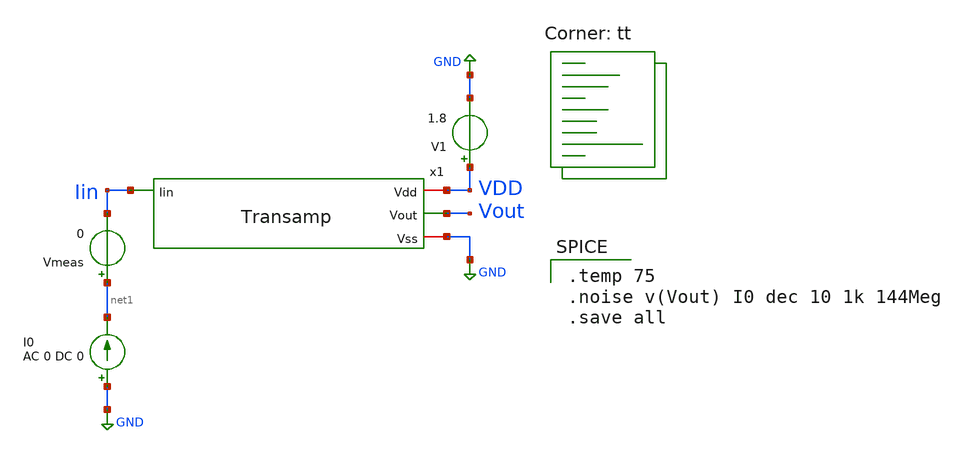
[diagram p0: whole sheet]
** sch_path: analog/library/TIAs/RGC-TIA/TIA_noise_tb.sch
**.subckt TIA_noise_tb
x1 VDD Vout Iin GND Transamp
V1 VDD GND 1.8
I0 GND net1 AC 0 DC 0
Vmeas net1 Iin 0
.save i(vmeas)
**** begin user architecture code
.lib $::SKYWATER_MODELS/sky130.lib.spice tt

.temp 75
.noise v(Vout) I0 dec 10 1k 144Meg
.save all

**** end user architecture code
**.ends

* expanding   symbol:  Transamp.sym # of pins=4
** sym_path: analog/library/TIAs/RGC-TIA/Transamp.sym
** sch_path: analog/library/TIAs/RGC-TIA/Transamp.sch
.subckt Transamp Vdd Vout Iin Vss
*.ipin Iin
*.opin Vout
*.iopin Vss
*.iopin Vdd
R1 net1 Vdd sky130_fd_pr__res_generic_l1 W=0.20 L=32.8 m=1
R2 net2 Vdd sky130_fd_pr__res_generic_l1 W=0.20 L=32.8 m=1
R4 Vss Iin sky130_fd_pr__res_generic_l1 W=0.20 L=32.8 m=1
XM1 net1 net2 Iin Iin sky130_fd_pr__nfet_01v8_lvt L=0.5 W='12.5 * 10 ' nf=10 ad='int((10 + 1)/2) * 12.5 / 10 * 0.29'
+ as='int((10 + 2)/2) * 12.5 / 10 * 0.29' pd='2*int((10 + 1)/2) * (12.5 / 10 + 0.29)' ps='2*int((10 + 2)/2) * (12.5 / 10 + 0.29)'
+ nrd='0.29 / 12.5 ' nrs='0.29 / 12.5 ' sa=0 sb=0 sd=0 mult=1 m=1
XM2 net2 Iin Vss Vss sky130_fd_pr__nfet_01v8_lvt L=0.5 W='12.5 * 10 ' nf=10 ad='int((10 + 1)/2) * 12.5 / 10 * 0.29'
+ as='int((10 + 2)/2) * 12.5 / 10 * 0.29' pd='2*int((10 + 1)/2) * (12.5 / 10 + 0.29)' ps='2*int((10 + 2)/2) * (12.5 / 10 + 0.29)'
+ nrd='0.29 / 12.5 ' nrs='0.29 / 12.5 ' sa=0 sb=0 sd=0 mult=1 m=1
R3 Vout Vdd sky130_fd_pr__res_generic_l1 W=0.20 L=98.3 m=1
XM3 Vout net1 net3 net3 sky130_fd_pr__nfet_01v8_lvt L=0.5 W='12.5 * 10 ' nf=10 ad='int((10 + 1)/2) * 12.5 / 10 * 0.29'
+ as='int((10 + 2)/2) * 12.5 / 10 * 0.29' pd='2*int((10 + 1)/2) * (12.5 / 10 + 0.29)' ps='2*int((10 + 2)/2) * (12.5 / 10 + 0.29)'
+ nrd='0.29 / 12.5 ' nrs='0.29 / 12.5 ' sa=0 sb=0 sd=0 mult=1 m=1
R5 Vss net3 sky130_fd_pr__res_generic_l1 W=0.20 L=96.6 m=1
XC1 net3 Vss sky130_fd_pr__cap_mim_m3_1 W=12 L=6 MF=3 m=3
.ends

.GLOBAL GND
.end
